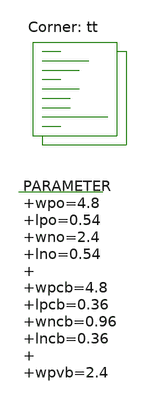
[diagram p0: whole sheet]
** sch_path: xschem/vco-tb.sch
**.subckt vco-tb
.param wpo=4.8 lpo=0.54 wno=2.4 lno=0.54 wpcb=4.8 lpcb=0.36 wncb=0.96 lncb=0.36 wpvb=2.4 lpvb=0.36
+ wnvc=96 lnvc=0.9 wpbuff=4.8 lpbuff=0.18 wnbuff=1.2 lnbuff=0.18 rin=100 rex=10k lres=3.5

**** begin user architecture code
 .lib $::SKYWATER_MODELS/sky130.lib.spice tt

.param mc_mm_switch = 0
.param mc_pr_switch = 0




  .option wnflag=1
  .option safecurrents

  .param val=0.35
  .param lres=0.35

  Vvdd vdd  gnd dc 1.8
  Vcon vcon gnd dc 1.3

  .control
    reset
    save all
    write vco.raw
    set appendwrite
    let l_it = 0.35
    *while l_it <= 7.0
      alterparam lres = $&l_it
      reset
      save all
      tran 0.01n 150n
      write vco.raw
      let l_it = l_it + 0.35

      alterparam lres = $&l_it
      reset
      save all
      tran 0.01n 150n
      write vco.raw
      let l_it = l_it + 0.35

      alterparam lres = $&l_it
      reset
      save all
      tran 0.01n 150n
      write vco.raw
      let l_it = l_it + 0.35

      alterparam lres = $&l_it
      reset
      save all
      tran 0.01n 150n
      write vco.raw
      let l_it = l_it + 0.35

      alterparam lres = $&l_it
      reset
      save all
      tran 0.01n 150n
      write vco.raw
      let l_it = l_it + 0.35

      alterparam lres = $&l_it
      reset
      save all
      tran 0.01n 150n
      write vco.raw
      let l_it = l_it + 0.35

      alterparam lres = $&l_it
      reset
      save all
      tran 0.01n 150n
      write vco.raw
      let l_it = l_it + 0.35

      alterparam lres = $&l_it
      reset
      save all
      tran 0.01n 150n
      write vco.raw
      let l_it = l_it + 0.35

      alterparam lres = $&l_it
      reset
      save all
      tran 0.01n 150n
      write vco.raw
      let l_it = l_it + 0.35

      alterparam lres = $&l_it
      reset
      save all
      tran 0.01n 150n
      write vco.raw
      let l_it = l_it + 0.35
    *end
    quit 0
  .endc



**** end user architecture code
**.ends
.end
